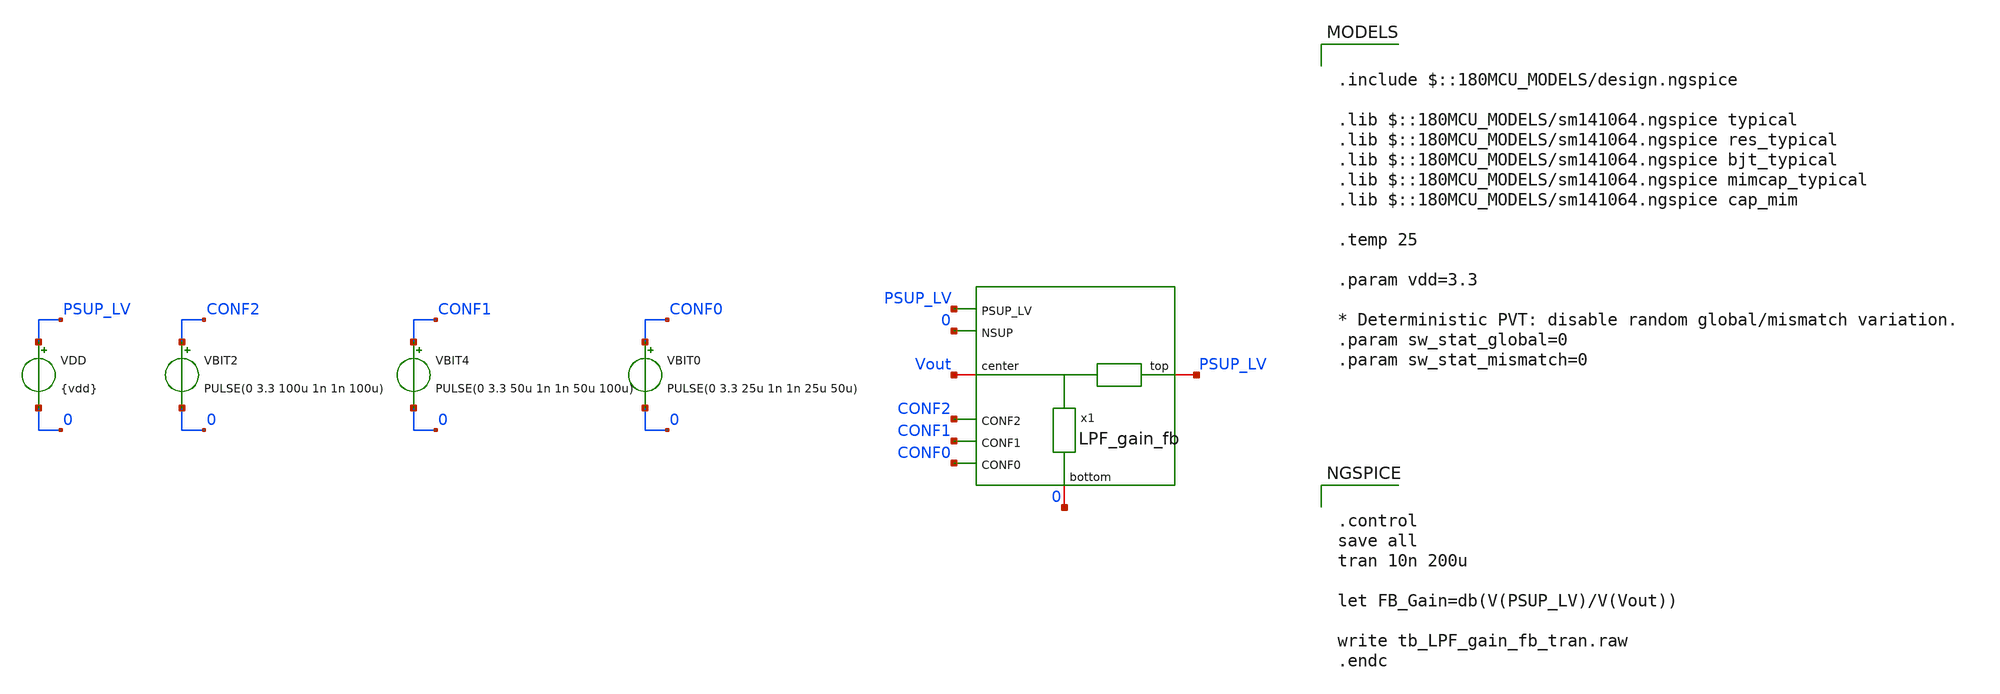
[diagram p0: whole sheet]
** sch_path: xschem/blocks/LPF_gain_fb/tb_LPF_gain_fb_tran.sch
**.subckt tb_LPF_gain_fb_tran
VBIT0 CONF0 0 PULSE(0 3.3 25u 1n 1n 25u 50u)
VBIT4 CONF1 0 PULSE(0 3.3 50u 1n 1n 50u 100u)
VDD PSUP_LV 0 {vdd}
VBIT2 CONF2 0 PULSE(0 3.3 100u 1n 1n 100u)
x1 PSUP_LV Vout PSUP_LV 0 CONF2 CONF1 CONF0 0 LPF_gain_fb
**** begin user architecture code

.include $::180MCU_MODELS/design.ngspice

.lib $::180MCU_MODELS/sm141064.ngspice typical
.lib $::180MCU_MODELS/sm141064.ngspice res_typical
.lib $::180MCU_MODELS/sm141064.ngspice bjt_typical
.lib $::180MCU_MODELS/sm141064.ngspice mimcap_typical
.lib $::180MCU_MODELS/sm141064.ngspice cap_mim

.temp 25

.param vdd=3.3

* Deterministic PVT: disable random global/mismatch variation.
.param sw_stat_global=0
.param sw_stat_mismatch=0



.control
save all
tran 10n 200u

let FB_Gain=db(V(PSUP_LV)/V(Vout))

write tb_LPF_gain_fb_tran.raw
.endc


**** end user architecture code
**.ends

* expanding   symbol:  blocks/LPF_gain_fb/LPF_gain_fb.sym # of pins=8
** sym_path: xschem/blocks/LPF_gain_fb/LPF_gain_fb.sym
** sch_path: xschem/blocks/LPF_gain_fb/LPF_gain_fb.sch
.subckt LPF_gain_fb top center PSUP_LV NSUP CONF2 CONF1 CONF0 bottom
*.iopin top
*.iopin center
*.iopin bottom
*.ipin PSUP_LV
*.ipin NSUP
*.ipin CONF1
*.ipin CONF2
*.ipin CONF0
x13 nC6 nCONF0 CONF2 PSUP_LV NSUP CONF1 nand_3
x14 nC5 CONF0 CONF2 PSUP_LV NSUP nCONF1 nand_3
x15 nC4 nCONF0 CONF2 PSUP_LV NSUP nCONF1 nand_3
x16 nC3 CONF0 nCONF2 PSUP_LV NSUP CONF1 nand_3
x17 nC2 nCONF0 nCONF2 PSUP_LV NSUP CONF1 nand_3
x18 nC1 CONF0 nCONF2 PSUP_LV NSUP nCONF1 nand_3
x19 nC0 nCONF0 nCONF2 PSUP_LV NSUP nCONF1 nand_3
* noconn NSUP
* noconn PSUP_LV
x21 PSUP_LV nC6 C6 NSUP not
x22 PSUP_LV nC5 C5 NSUP not
* noconn NSUP
* noconn PSUP_LV
x26 PSUP_LV nC4 C4 NSUP not
x27 PSUP_LV nC3 C3 NSUP not
x28 PSUP_LV nC2 C2 NSUP not
x29 PSUP_LV nC1 C1 NSUP not
x30 PSUP_LV nC0 C0 NSUP not
* noconn NSUP
* noconn PSUP_LV
x3 PSUP_LV CONF0 nCONF0 NSUP not
x6 PSUP_LV CONF1 nCONF1 NSUP not
x7 PSUP_LV CONF2 nCONF2 NSUP not
x4 nC7 CONF0 CONF2 PSUP_LV NSUP CONF1 nand_3
x8 PSUP_LV nC7 C7 NSUP not
x1 C0 center top nC0 PSUP_LV NSUP transmission_gate_alt
x2 C1 center TAP_1 nC1 PSUP_LV NSUP transmission_gate_alt
x5 C2 center TAP_2 nC2 PSUP_LV NSUP transmission_gate_alt
x9 C3 center TAP_3 nC3 PSUP_LV NSUP transmission_gate_alt
x10 C4 center TAP_4 nC4 PSUP_LV NSUP transmission_gate_alt
x11 C5 center TAP_5 nC5 PSUP_LV NSUP transmission_gate_alt
x12 C6 center TAP_6 nC6 PSUP_LV NSUP transmission_gate_alt
x20 C7 center TAP_7 nC7 PSUP_LV NSUP transmission_gate_alt
XR9 TAP_6 TAP_5 PSUP_LV ppolyf_u_1k r_width=1e-6 r_length=59e-6 m=1
XR10 bottom TAP_7 PSUP_LV ppolyf_u_1k r_width=1e-6 r_length=133e-6 m=1
XR11 TAP_5 TAP_4 PSUP_LV ppolyf_u_1k r_width=1e-6 r_length=79e-6 m=1
XR12 TAP_4 TAP_3 PSUP_LV ppolyf_u_1k r_width=1e-6 r_length=105e-6 m=1
XR13 TAP_3 TAP_2 PSUP_LV ppolyf_u_1k r_width=1e-6 r_length=140e-6 m=1
XR14 TAP_2 TAP_1 PSUP_LV ppolyf_u_1k r_width=1e-6 r_length=187e-6 m=1
XR15 TAP_1 top PSUP_LV ppolyf_u_1k r_width=1e-6 r_length=249e-6 m=1
XR16 TAP_7 TAP_6 PSUP_LV ppolyf_u_1k r_width=1e-6 r_length=44e-6 m=1
.ends


* expanding   symbol:  blocks/nand_3/nand_3.sym # of pins=8
** sym_path: xschem/blocks/nand_3/nand_3.sym
** sch_path: xschem/blocks/nand_3/nand_3.sch
.subckt nand_3 Y A C PSUP NSUP B
*.ipin PSUP
*.ipin NSUP
*.ipin A
*.ipin B
*.opin Y
*.ipin C
XM5 net1 C NSUP NSUP nfet_03v3 L=0.28u W=0.22u nf=1 ad='int((nf+1)/2) * W/nf * 0.18u' as='int((nf+2)/2) * W/nf * 0.18u'
+ pd='2*int((nf+1)/2) * (W/nf + 0.18u)' ps='2*int((nf+2)/2) * (W/nf + 0.18u)' nrd='0.18u / W' nrs='0.18u / W'
+ sa=0 sb=0 sd=0 m=1
XM1 Y A net2 NSUP nfet_03v3 L=0.28u W=0.22u nf=1 ad='int((nf+1)/2) * W/nf * 0.18u' as='int((nf+2)/2) * W/nf * 0.18u'
+ pd='2*int((nf+1)/2) * (W/nf + 0.18u)' ps='2*int((nf+2)/2) * (W/nf + 0.18u)' nrd='0.18u / W' nrs='0.18u / W'
+ sa=0 sb=0 sd=0 m=1
XM2 Y C PSUP PSUP pfet_03v3 L=0.28u W=0.5u nf=1 ad='int((nf+1)/2) * W/nf * 0.18u' as='int((nf+2)/2) * W/nf * 0.18u'
+ pd='2*int((nf+1)/2) * (W/nf + 0.18u)' ps='2*int((nf+2)/2) * (W/nf + 0.18u)' nrd='0.18u / W' nrs='0.18u / W'
+ sa=0 sb=0 sd=0 m=1
XM3 Y B PSUP PSUP pfet_03v3 L=0.28u W=0.5u nf=1 ad='int((nf+1)/2) * W/nf * 0.18u' as='int((nf+2)/2) * W/nf * 0.18u'
+ pd='2*int((nf+1)/2) * (W/nf + 0.18u)' ps='2*int((nf+2)/2) * (W/nf + 0.18u)' nrd='0.18u / W' nrs='0.18u / W'
+ sa=0 sb=0 sd=0 m=1
XM4 net2 B net1 NSUP nfet_03v3 L=0.28u W=0.22u nf=1 ad='int((nf+1)/2) * W/nf * 0.18u' as='int((nf+2)/2) * W/nf * 0.18u'
+ pd='2*int((nf+1)/2) * (W/nf + 0.18u)' ps='2*int((nf+2)/2) * (W/nf + 0.18u)' nrd='0.18u / W' nrs='0.18u / W'
+ sa=0 sb=0 sd=0 m=1
XM6 Y A PSUP PSUP pfet_03v3 L=0.28u W=0.5u nf=1 ad='int((nf+1)/2) * W/nf * 0.18u' as='int((nf+2)/2) * W/nf * 0.18u'
+ pd='2*int((nf+1)/2) * (W/nf + 0.18u)' ps='2*int((nf+2)/2) * (W/nf + 0.18u)' nrd='0.18u / W' nrs='0.18u / W'
+ sa=0 sb=0 sd=0 m=1
.ends


* expanding   symbol:  blocks/not/not.sym # of pins=6
** sym_path: xschem/blocks/not/not.sym
** sch_path: xschem/blocks/not/not.sch
.subckt not PSUP A B NSUP
*.ipin PSUP
*.ipin NSUP
*.ipin A
*.opin B
XM2 B A NSUP NSUP nfet_03v3 L=0.28u W=0.22u nf=1 ad='int((nf+1)/2) * W/nf * 0.18u' as='int((nf+2)/2) * W/nf * 0.18u'
+ pd='2*int((nf+1)/2) * (W/nf + 0.18u)' ps='2*int((nf+2)/2) * (W/nf + 0.18u)' nrd='0.18u / W' nrs='0.18u / W'
+ sa=0 sb=0 sd=0 m=1
XM1 B A PSUP PSUP pfet_03v3 L=0.28u W=0.5u nf=1 ad='int((nf+1)/2) * W/nf * 0.18u' as='int((nf+2)/2) * W/nf * 0.18u'
+ pd='2*int((nf+1)/2) * (W/nf + 0.18u)' ps='2*int((nf+2)/2) * (W/nf + 0.18u)' nrd='0.18u / W' nrs='0.18u / W'
+ sa=0 sb=0 sd=0 m=1
.ends


* expanding   symbol:  blocks/transmission_gate/transmission_gate_alt.sym # of pins=8
** sym_path: xschem/blocks/transmission_gate/transmission_gate_alt.sym
** sch_path: xschem/blocks/transmission_gate/transmission_gate_alt.sch
.subckt transmission_gate_alt C A B nC VPOS VNEG
*.iopin A
*.iopin B
*.ipin C
*.ipin nC
*.ipin VPOS
*.ipin VNEG
x1 C A B nC VPOS VNEG transmission_gate
.ends


* expanding   symbol:  blocks/transmission_gate/transmission_gate.sym # of pins=6
** sym_path: xschem/blocks/transmission_gate/transmission_gate.sym
** sch_path: xschem/blocks/transmission_gate/transmission_gate.sch
.subckt transmission_gate C A B nC VPOS VNEG
*.iopin A
*.iopin B
*.ipin C
*.ipin nC
*.ipin VPOS
*.ipin VNEG
XM3 A C B VNEG nfet_03v3 L=2u W=10u nf=1 ad='int((nf+1)/2) * W/nf * 0.18u' as='int((nf+2)/2) * W/nf * 0.18u'
+ pd='2*int((nf+1)/2) * (W/nf + 0.18u)' ps='2*int((nf+2)/2) * (W/nf + 0.18u)' nrd='0.18u / W' nrs='0.18u / W'
+ sa=0 sb=0 sd=0 m=2
XM4 A nC B VPOS pfet_03v3 L=2u W=10u nf=1 ad='int((nf+1)/2) * W/nf * 0.18u' as='int((nf+2)/2) * W/nf * 0.18u'
+ pd='2*int((nf+1)/2) * (W/nf + 0.18u)' ps='2*int((nf+2)/2) * (W/nf + 0.18u)' nrd='0.18u / W' nrs='0.18u / W'
+ sa=0 sb=0 sd=0 m=4
.ends

.end
